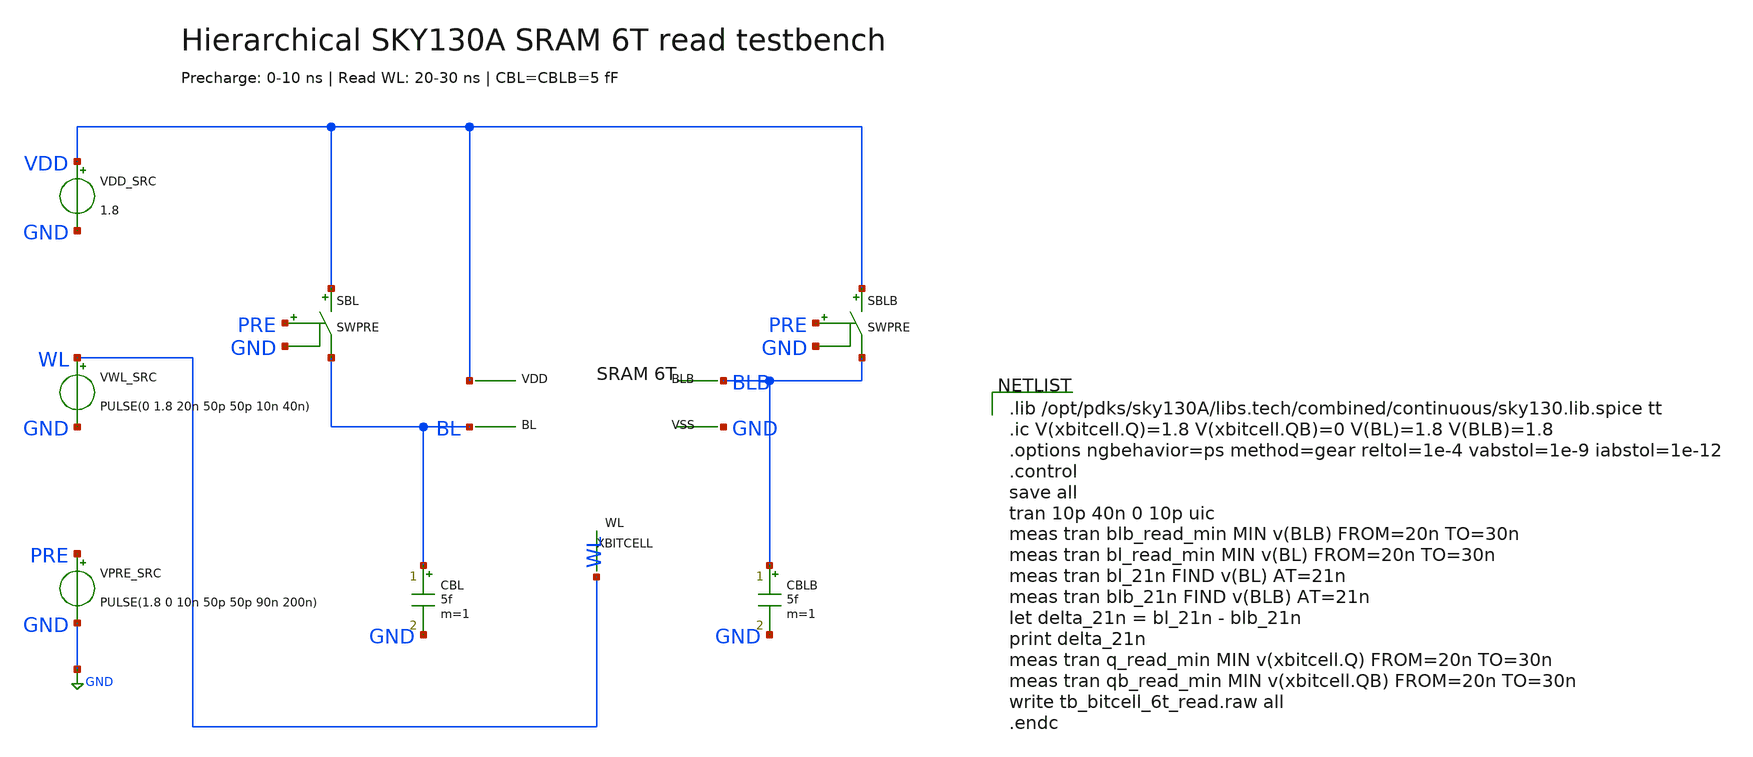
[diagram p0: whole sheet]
** sch_path: sims/bitcell_6t/tb_bitcell_6t_read.sch
**.subckt tb_bitcell_6t_read
XBITCELL VDD BL BLB GND WL bitcell_6t WPU=0.42 WPD=0.42 WACC=0.42
VDD_SRC VDD GND 1.8
VWL_SRC WL GND PULSE(0 1.8 20n 50p 50p 10n 40n)
VPRE_SRC PRE GND PULSE(1.8 0 10n 50p 50p 90n 200n)
SBL VDD BL PRE GND SWPRE
SBLB VDD BLB PRE GND SWPRE
CBL BL GND 5f m=1
CBLB BLB GND 5f m=1
**** begin user architecture code

.lib /opt/pdks/sky130A/libs.tech/combined/continuous/sky130.lib.spice tt
.ic V(xbitcell.Q)=1.8 V(xbitcell.QB)=0 V(BL)=1.8 V(BLB)=1.8
.options ngbehavior=ps method=gear reltol=1e-4 vabstol=1e-9 iabstol=1e-12
.control
save all
tran 10p 40n 0 10p uic
meas tran blb_read_min MIN v(BLB) FROM=20n TO=30n
meas tran bl_read_min MIN v(BL) FROM=20n TO=30n
meas tran bl_21n FIND v(BL) AT=21n
meas tran blb_21n FIND v(BLB) AT=21n
let delta_21n = bl_21n - blb_21n
print delta_21n
meas tran q_read_min MIN v(xbitcell.Q) FROM=20n TO=30n
meas tran qb_read_min MIN v(xbitcell.QB) FROM=20n TO=30n
write tb_bitcell_6t_read.raw all
.endc

**** end user architecture code
**.ends
.GLOBAL GND
**** begin user architecture code
.model SWPRE SW(RON=10 ROFF=1e12 VT=0.9 VH=0.1)
**** end user architecture code
.end
